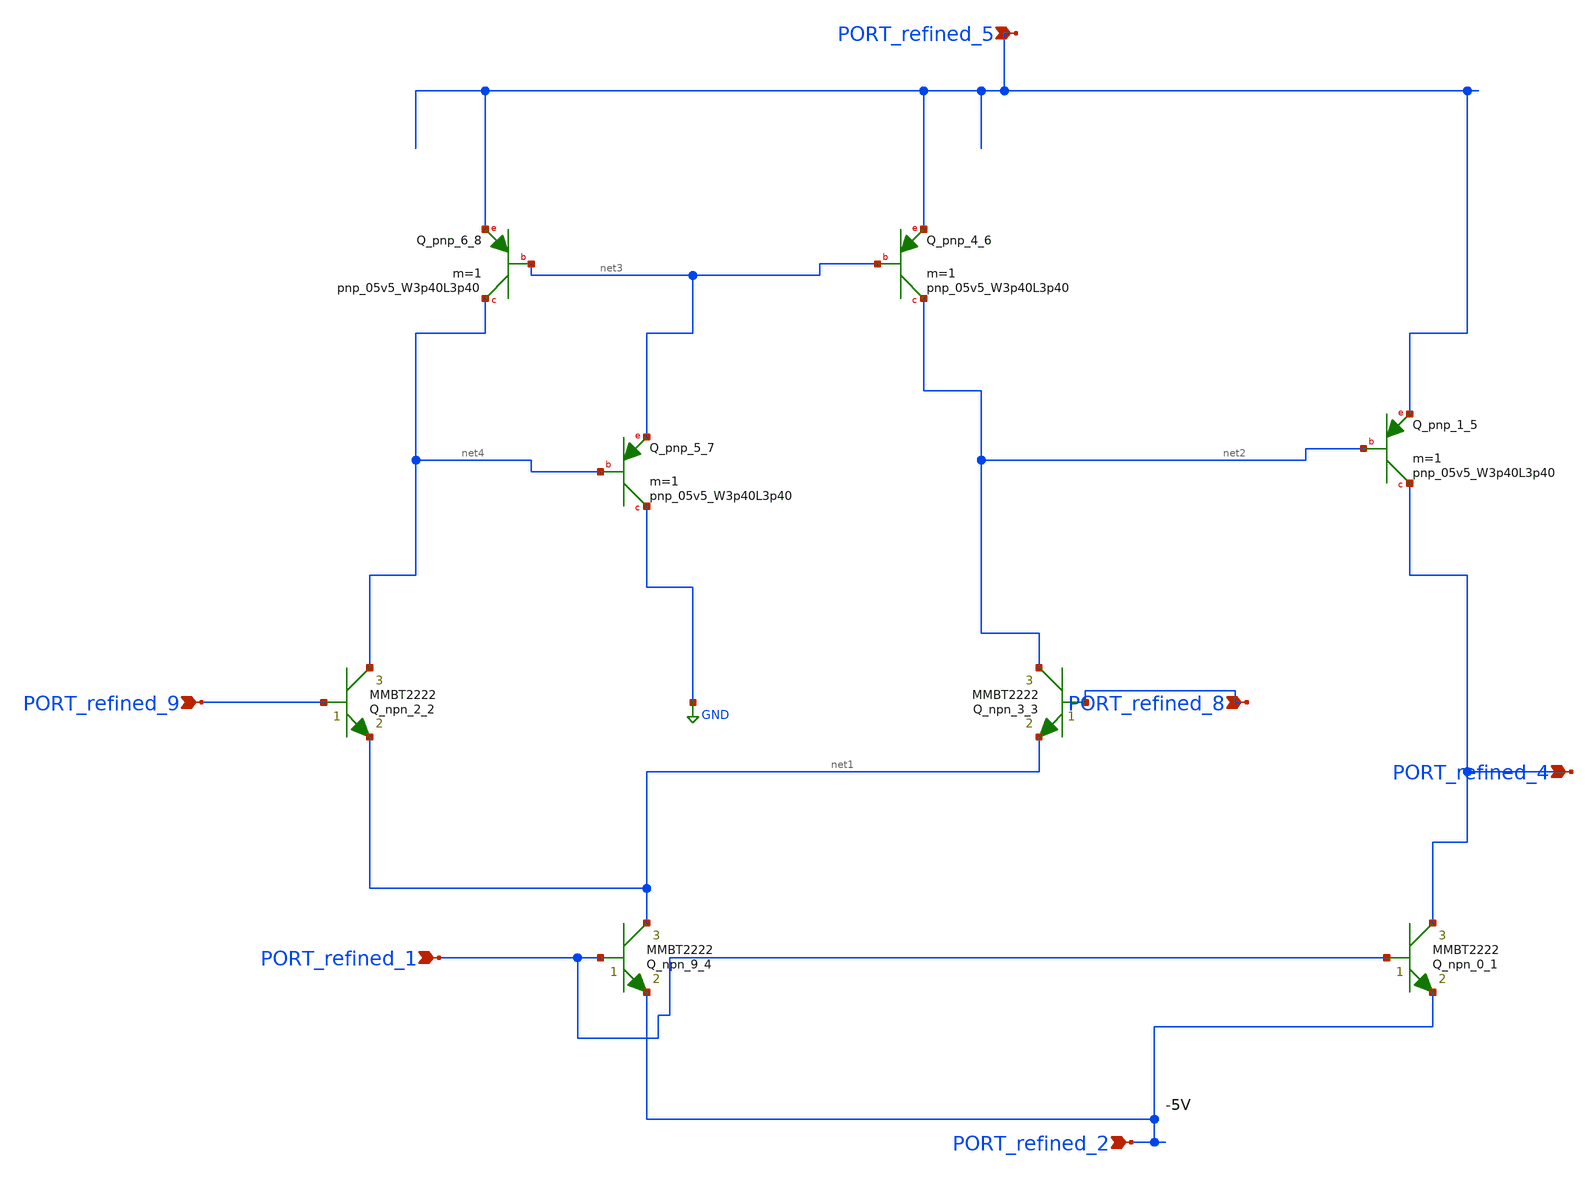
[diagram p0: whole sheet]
** sch_path: schematics/Image2Net/072.sch
**.subckt 072 PORT_refined_8 PORT_refined_9 PORT_refined_1 PORT_refined_4 PORT_refined_2
*+ PORT_refined_5
*.ipin PORT_refined_8
*.ipin PORT_refined_9
*.ipin PORT_refined_1
*.ipin PORT_refined_4
*.ipin PORT_refined_2
*.ipin PORT_refined_5
Q_npn_0_1 PORT_refined_4 PORT_refined_1 PORT_refined_2 MMBT2222 area=1 m=1
Q_npn_2_2 net4 PORT_refined_9 net1 MMBT2222 area=1 m=1
Q_npn_3_3 net2 PORT_refined_8 net1 MMBT2222 area=1 m=1
Q_npn_9_4 net1 PORT_refined_1 PORT_refined_2 MMBT2222 area=1 m=1
XQ_pnp_1_5 PORT_refined_4 net2 PORT_refined_5 sky130_fd_pr__pnp_05v5_W3p40L3p40 m=1
XQ_pnp_4_6 net2 net3 PORT_refined_5 sky130_fd_pr__pnp_05v5_W3p40L3p40 m=1
XQ_pnp_5_7 GND net4 net3 sky130_fd_pr__pnp_05v5_W3p40L3p40 m=1
XQ_pnp_6_8 net4 net3 PORT_refined_5 sky130_fd_pr__pnp_05v5_W3p40L3p40 m=1
**.ends
.GLOBAL GND
.end
